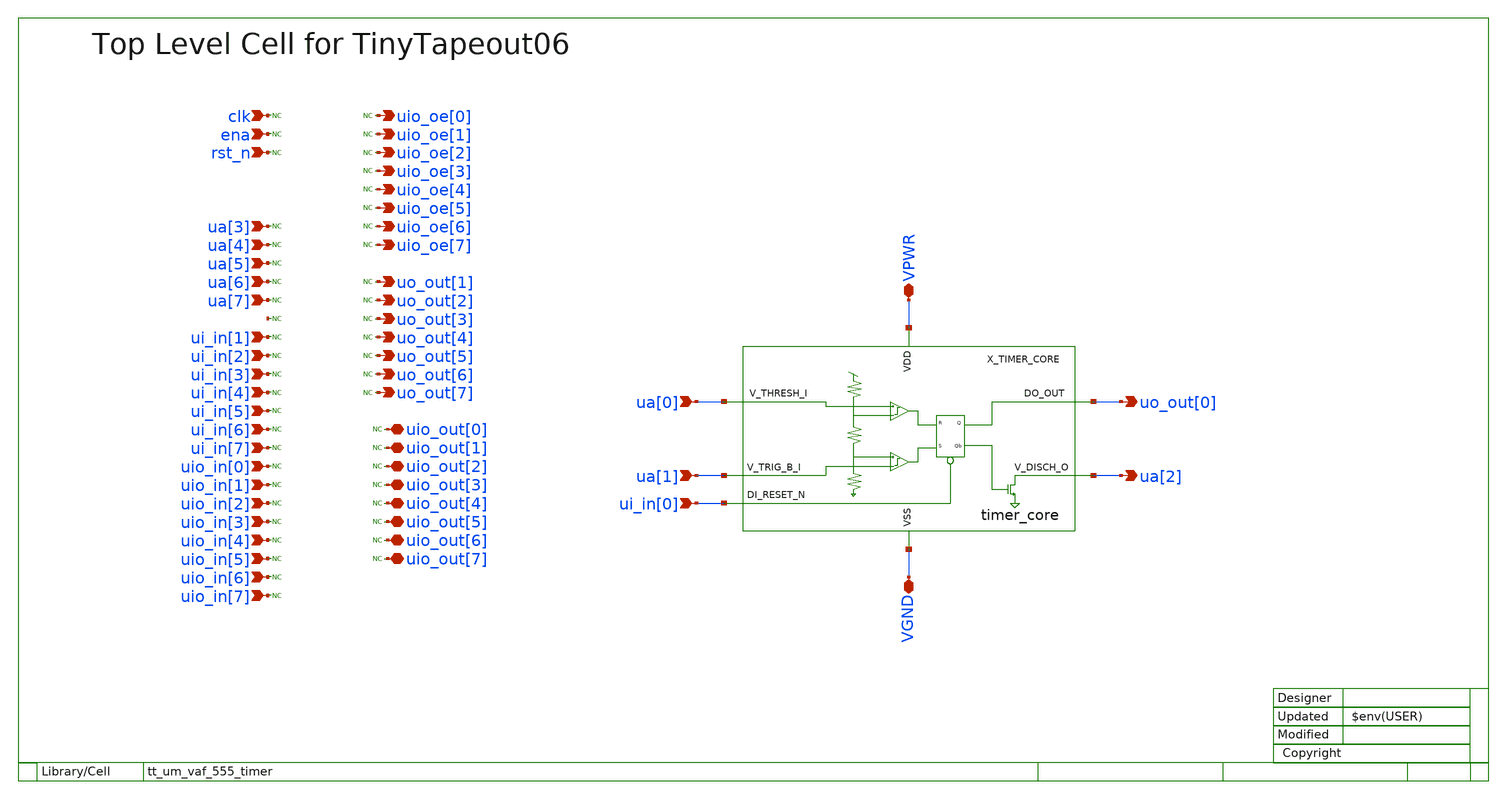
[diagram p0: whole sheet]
** sch_path: xsch/ip/top/tt_um_vaf_555_timer/tt_um_vaf_555_timer.sch
**.subckt tt_um_vaf_555_timer VPWR VGND clk ena rst_n ua[0] ua[1] ua[3] ua[4] ua[5] ua[6] ua[7]
*+ ui_in[0] ui_in[1] ui_in[2] ui_in[3] ui_in[4] ui_in[5] ui_in[6] ui_in[7] uio_in[0] uio_in[1] uio_in[2]
*+ uio_in[3] uio_in[4] uio_in[5] uio_in[6] uio_in[7] uio_oe[0] uio_oe[1] uio_oe[2] uio_oe[3] uio_oe[4] uio_oe[5]
*+ uio_oe[6] uio_oe[7] uo_out[0] uo_out[1] uo_out[2] uo_out[3] uo_out[4] uo_out[5] uo_out[6] uo_out[7]
*+ uio_out[0] uio_out[1] uio_out[2] uio_out[3] uio_out[4] uio_out[5] uio_out[6] uio_out[7] ua[2]
*.iopin VPWR
*.iopin VGND
*.ipin clk
*.ipin ena
*.ipin rst_n
*.ipin ua[0]
*.ipin ua[1]
*.ipin ua[3]
*.ipin ua[4]
*.ipin ua[5]
*.ipin ua[6]
*.ipin ua[7]
*.ipin ui_in[0]
*.ipin ui_in[1]
*.ipin ui_in[2]
*.ipin ui_in[3]
*.ipin ui_in[4]
*.ipin ui_in[5]
*.ipin ui_in[6]
*.ipin ui_in[7]
*.ipin uio_in[0]
*.ipin uio_in[1]
*.ipin uio_in[2]
*.ipin uio_in[3]
*.ipin uio_in[4]
*.ipin uio_in[5]
*.ipin uio_in[6]
*.ipin uio_in[7]
*.opin uio_oe[0]
*.opin uio_oe[1]
*.opin uio_oe[2]
*.opin uio_oe[3]
*.opin uio_oe[4]
*.opin uio_oe[5]
*.opin uio_oe[6]
*.opin uio_oe[7]
*.opin uo_out[0]
*.opin uo_out[1]
*.opin uo_out[2]
*.opin uo_out[3]
*.opin uo_out[4]
*.opin uo_out[5]
*.opin uo_out[6]
*.opin uo_out[7]
*.iopin uio_out[0]
*.iopin uio_out[1]
*.iopin uio_out[2]
*.iopin uio_out[3]
*.iopin uio_out[4]
*.iopin uio_out[5]
*.iopin uio_out[6]
*.iopin uio_out[7]
*.opin ua[2]
* noconn clk
* noconn ena
* noconn rst_n
* noconn ua[3]
* noconn ua[6]
* noconn #net1
* noconn ui_in[1]
* noconn ui_in[2]
* noconn ui_in[3]
* noconn ui_in[4]
* noconn ui_in[5]
* noconn ui_in[6]
* noconn ui_in[7]
* noconn uio_in[0]
* noconn uio_in[1]
* noconn uio_in[2]
* noconn uio_in[3]
* noconn uio_in[4]
* noconn uio_in[5]
* noconn uio_in[6]
* noconn uio_in[7]
* noconn uio_oe[0]
* noconn uio_oe[1]
* noconn uio_oe[2]
* noconn uio_oe[3]
* noconn uio_oe[4]
* noconn uio_oe[5]
* noconn uio_oe[6]
* noconn uio_oe[7]
* noconn uo_out[1]
* noconn uo_out[2]
* noconn uo_out[3]
* noconn uo_out[4]
* noconn uo_out[5]
* noconn uo_out[6]
* noconn uo_out[7]
* noconn uio_out[0]
* noconn uio_out[1]
* noconn uio_out[2]
* noconn uio_out[3]
* noconn uio_out[4]
* noconn uio_out[5]
* noconn uio_out[6]
* noconn uio_out[7]
X_TIMER_CORE ua[0] ua[1] ui_in[0] uo_out[0] ua[2] VPWR VGND timer_core
* noconn ua[5]
* noconn ua[4]
* noconn ua[7]
**.ends
.end
